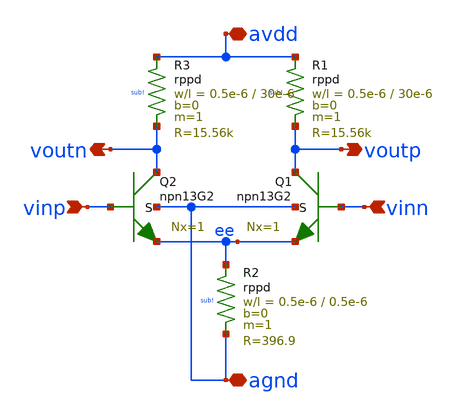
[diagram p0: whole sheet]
** sch_path: xschem/comparator.sch
**.subckt comparator avdd vinp voutp agnd vinn voutn
*.iopin avdd
*.ipin vinp
*.opin voutp
*.iopin agnd
*.ipin vinn
*.opin voutn
XQ1 voutp vinn ee agnd npn13G2 Nx=1 mm_ok=1
XR1 avdd voutp sub! rppd w=0.5e-6 l=30e-6 m=1 b=0 mm_ok=1
XR2 ee agnd sub! rppd w=0.5e-6 l=0.5e-6 m=1 b=0 mm_ok=1
XR3 avdd voutn sub! rppd w=0.5e-6 l=30e-6 m=1 b=0 mm_ok=1
XQ2 voutn vinp ee agnd npn13G2 Nx=1 mm_ok=1
**.ends
.end
